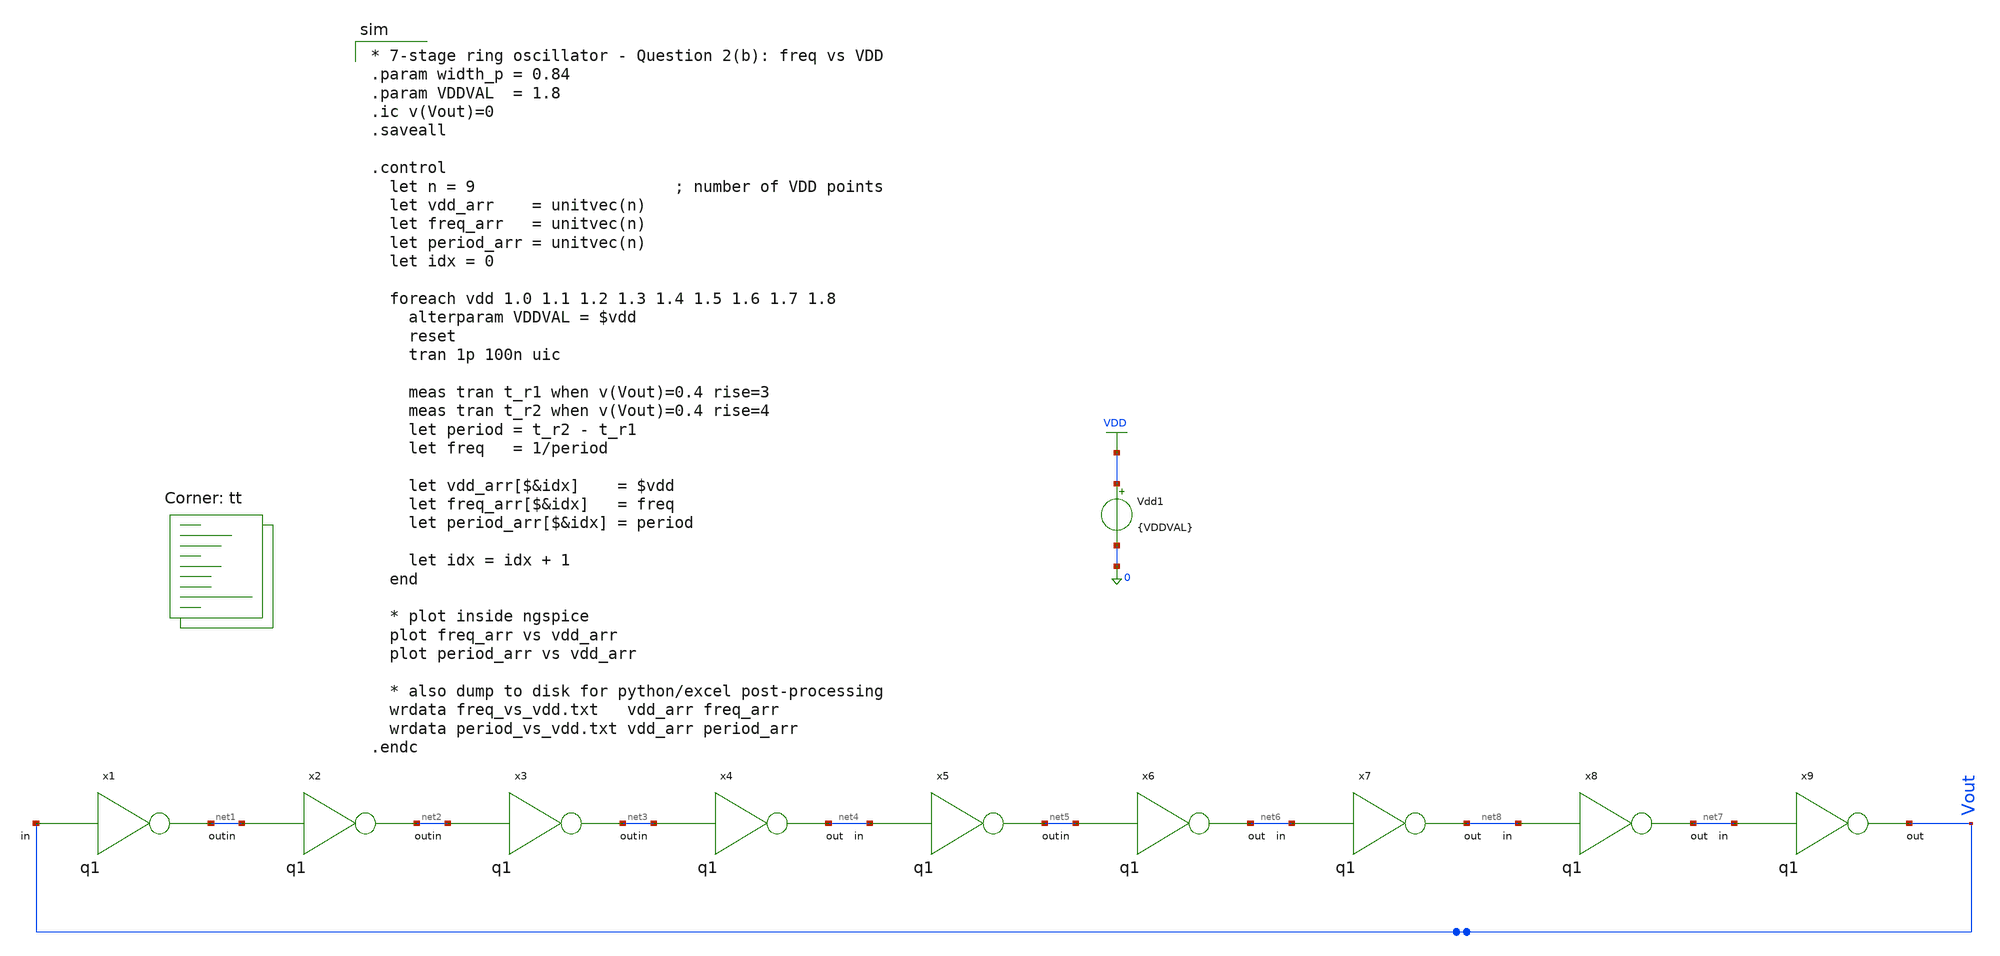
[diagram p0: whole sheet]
** sch_path: tutorial-3/source/q2c.sch
**.subckt q2c
x1 net1 Vout q1
x2 net2 net1 q1
x3 net3 net2 q1
x4 net4 net3 q1
x5 net5 net4 q1
x6 net6 net5 q1
x7 net8 net6 q1
Vdd1 VDD 0 {VDDVAL}
x8 net7 net8 q1
x9 Vout net7 q1
**** begin user architecture code

* 7-stage ring oscillator - Question 2(b): freq vs VDD
.param width_p = 0.84
.param VDDVAL  = 1.8
.ic v(Vout)=0
.saveall

.control
  let n = 9                     ; number of VDD points
  let vdd_arr    = unitvec(n)
  let freq_arr   = unitvec(n)
  let period_arr = unitvec(n)
  let idx = 0

  foreach vdd 1.0 1.1 1.2 1.3 1.4 1.5 1.6 1.7 1.8
    alterparam VDDVAL = $vdd
    reset
    tran 1p 100n uic

    meas tran t_r1 when v(Vout)=0.4 rise=3
    meas tran t_r2 when v(Vout)=0.4 rise=4
    let period = t_r2 - t_r1
    let freq   = 1/period

    let vdd_arr[$&idx]    = $vdd
    let freq_arr[$&idx]   = freq
    let period_arr[$&idx] = period

    let idx = idx + 1
  end

  * plot inside ngspice
  plot freq_arr vs vdd_arr
  plot period_arr vs vdd_arr

  * also dump to disk for python/excel post-processing
  wrdata freq_vs_vdd.txt   vdd_arr freq_arr
  wrdata period_vs_vdd.txt vdd_arr period_arr
.endc

.lib $::SKYWATER_MODELS/sky130.lib.spice tt
**** end user architecture code
**.ends

* expanding   symbol:  q1.sym # of pins=2
** sym_path: tutorial-3/source/q1.sym
** sch_path: tutorial-3/source/q1.sch
.subckt q1 out in
*.ipin in
*.opin out
XM1 out in VDD VDD sky130_fd_pr__pfet_01v8 L=0.15 W={width_p} nf=1 ad='int((nf+1)/2) * W/nf * 0.29' as='int((nf+2)/2) * W/nf * 0.29'
+ pd='2*int((nf+1)/2) * (W/nf + 0.29)' ps='2*int((nf+2)/2) * (W/nf + 0.29)' nrd='0.29 / W' nrs='0.29 / W'
+ sa=0 sb=0 sd=0 mult=1 m=1
XM2 out in GND GND sky130_fd_pr__nfet_01v8 L=0.15 W=0.42 nf=1 ad='int((nf+1)/2) * W/nf * 0.29' as='int((nf+2)/2) * W/nf * 0.29'
+ pd='2*int((nf+1)/2) * (W/nf + 0.29)' ps='2*int((nf+2)/2) * (W/nf + 0.29)' nrd='0.29 / W' nrs='0.29 / W'
+ sa=0 sb=0 sd=0 mult=1 m=1
.ends

.GLOBAL VDD
.GLOBAL GND
.end
